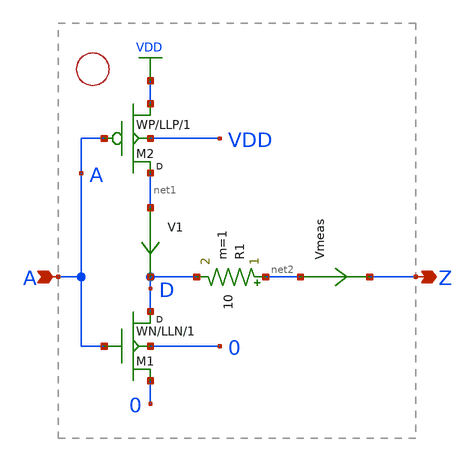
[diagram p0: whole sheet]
** sch_path: xschem_libs_newsym/examples/cmos_inv/schematic/cmos_inv.sch
* Copyright (C) 1998-2024 Stefan Frederik Schippers
* This program is free software; you can redistribute it and/or modify
* it under the terms of the GNU General Public License as published by
* the Free Software Foundation; either version 2 of the License, or
* (at your option) any later version.
* This program is distributed in the hope that it will be useful,
* but WITHOUT ANY WARRANTY; without even the implied warranty of
* MERCHANTABILITY or FITNESS FOR A PARTICULAR PURPOSE.  See the
* GNU General Public License for more details.
* You should have received a copy of the GNU General Public License
* along with this program; if not, write to the Free Software
**.subckt cmos_inv Z A
*.opin Z
*.ipin A
M2 net1 A VDD VDD p w=WP l=LLP m=1
M1 D A 0 0 n w=WN l=LLN m=1
R1 net2 D 10 m=1
V1 net1 D 0
.save i(v1)
Vmeas net2 Z 0
.save i(vmeas)
**.ends
.GLOBAL VDD
.end
